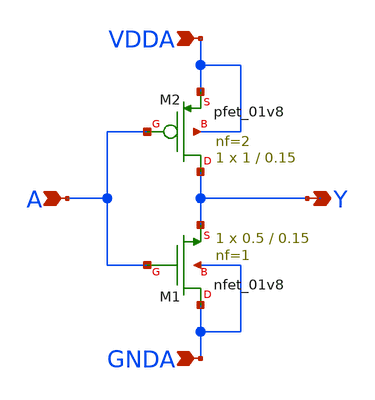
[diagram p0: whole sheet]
** sch_path: projects/pll/pfd/xschem_ngspice/inverter_pfd.sch
**.subckt inverter_pfd A Y VDDA GNDA
*.ipin A
*.opin Y
*.ipin VDDA
*.ipin GNDA
XM2 Y A VDDA VDDA sky130_fd_pr__pfet_01v8 L=0.15 W=1 nf=2 ad='int((nf+1)/2) * W/nf * 0.29' as='int((nf+2)/2) * W/nf * 0.29'
+ pd='2*int((nf+1)/2) * (W/nf + 0.29)' ps='2*int((nf+2)/2) * (W/nf + 0.29)' nrd='0.29 / W' nrs='0.29 / W'
+ sa=0 sb=0 sd=0 mult=1 m=1
XM1 GNDA A Y GNDA sky130_fd_pr__nfet_01v8 L=0.15 W=0.5 nf=1 ad='int((nf+1)/2) * W/nf * 0.29' as='int((nf+2)/2) * W/nf * 0.29'
+ pd='2*int((nf+1)/2) * (W/nf + 0.29)' ps='2*int((nf+2)/2) * (W/nf + 0.29)' nrd='0.29 / W' nrs='0.29 / W'
+ sa=0 sb=0 sd=0 mult=1 m=1
**.ends
.end
